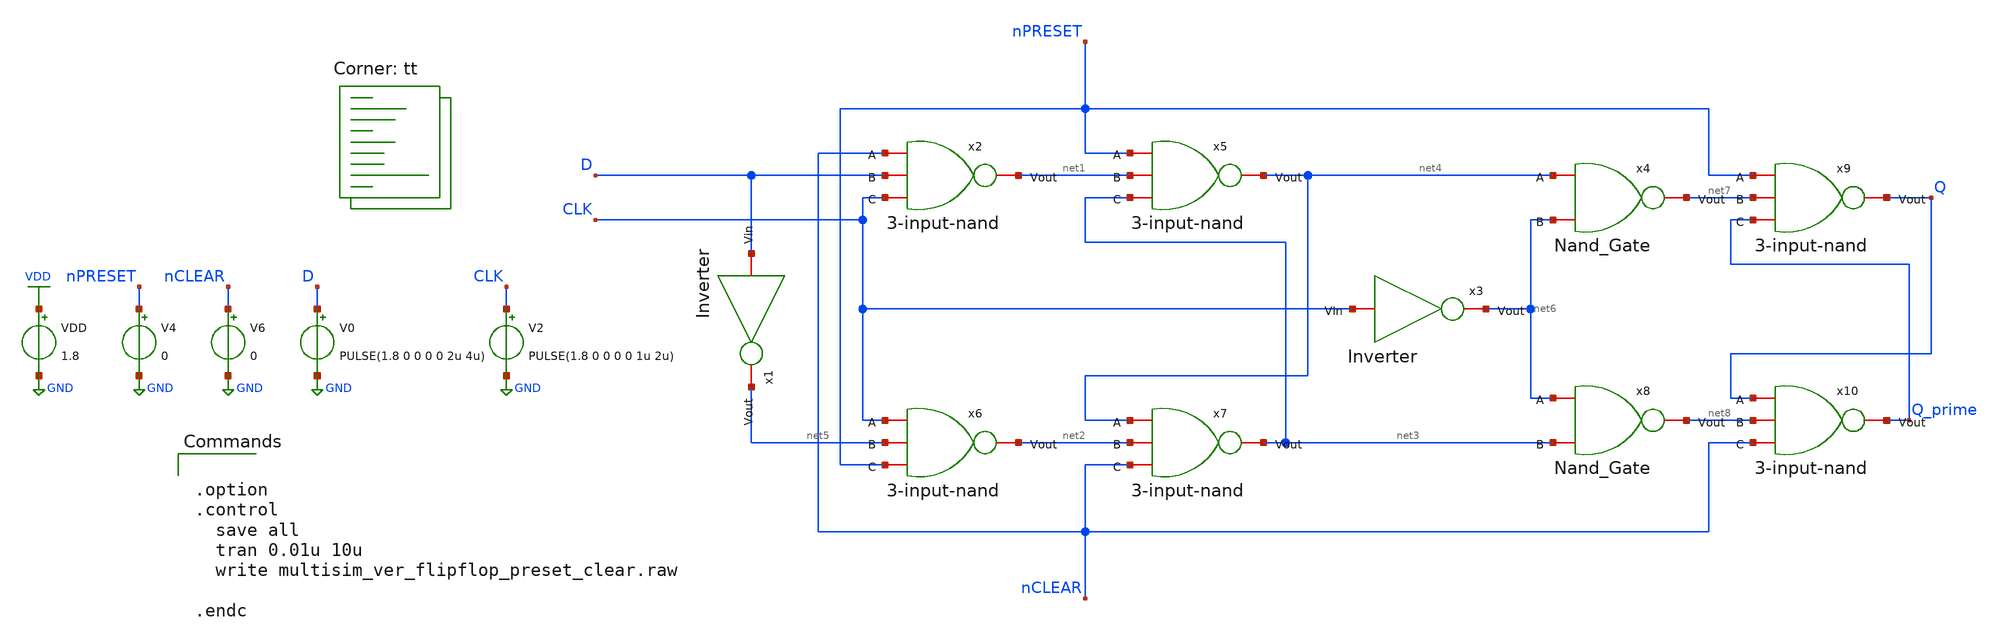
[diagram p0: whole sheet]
** sch_path: xschem/DAC/multisim_ver_flipflop_preset_clear.sch
**.subckt multisim_ver_flipflop_preset_clear
x1 D net5 Inverter
x2 CLK D nCLEAR net1 3-input-nand
x5 net3 net1 nPRESET net4 3-input-nand
x6 nPRESET net5 CLK net2 3-input-nand
x7 nCLEAR net2 net4 net3 3-input-nand
x3 CLK net6 Inverter
x4 net6 net4 net7 Nand_Gate
x8 net3 net6 net8 Nand_Gate
x9 Q_prime net7 nPRESET Q 3-input-nand
x10 nCLEAR net8 Q Q_prime 3-input-nand
V2 CLK GND PULSE(1.8 0 0 0 0 1u 2u)
V4 nPRESET GND 0
V6 nCLEAR GND 0
V0 D GND PULSE(1.8 0 0 0 0 2u 4u)
VDD VDD GND 1.8
**** begin user architecture code


.option
.control
  save all
  tran 0.01u 10u
  write multisim_ver_flipflop_preset_clear.raw

.endc


.lib $::SKYWATER_MODELS/sky130.lib.spice tt
**** end user architecture code
**.ends
.GLOBAL GND
.GLOBAL VDD
.end
